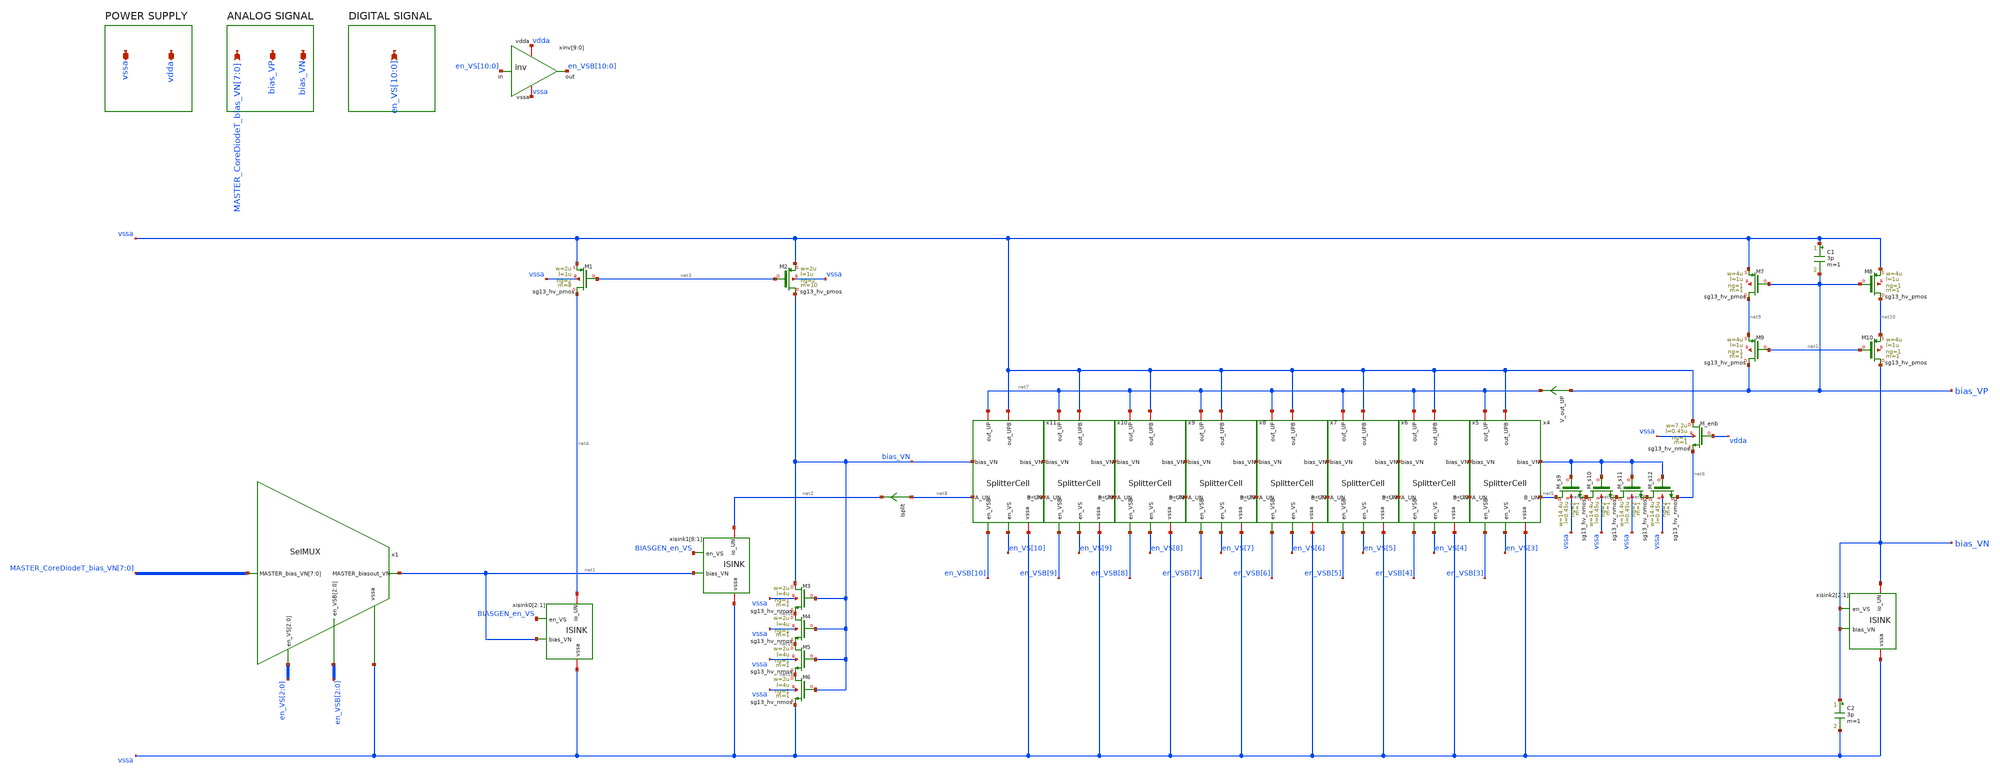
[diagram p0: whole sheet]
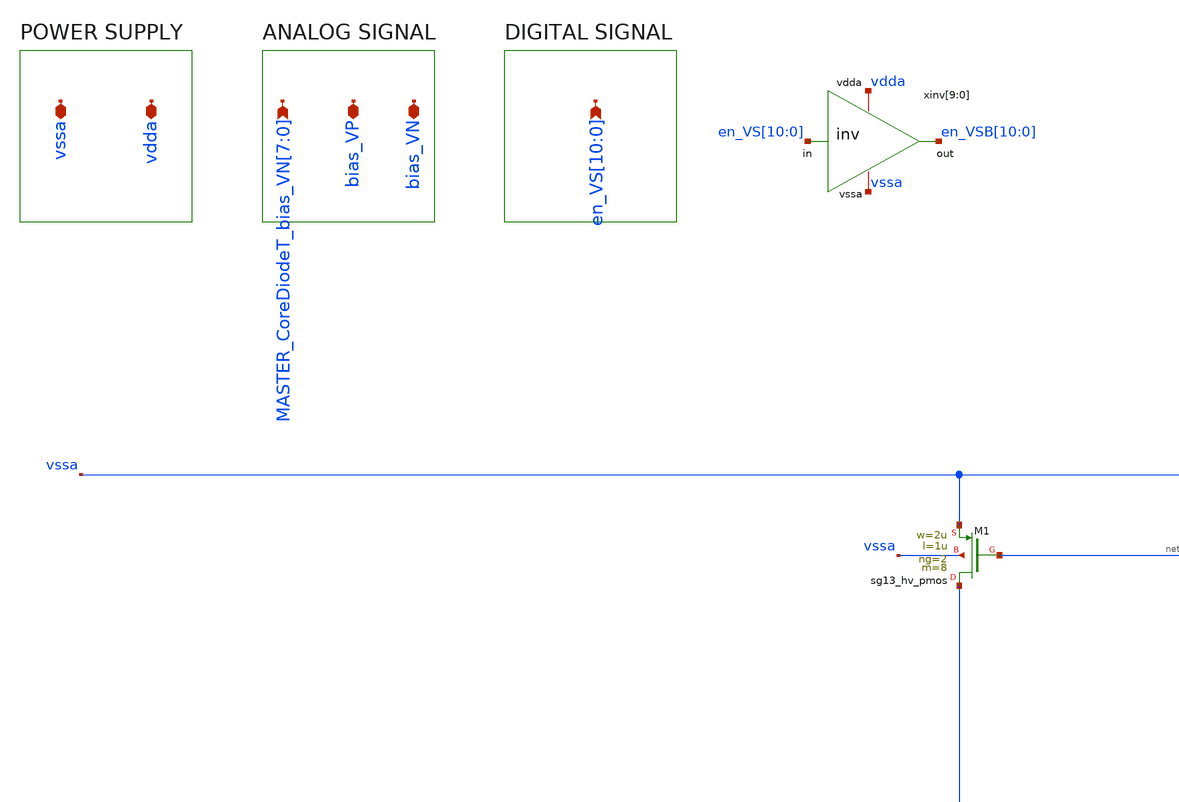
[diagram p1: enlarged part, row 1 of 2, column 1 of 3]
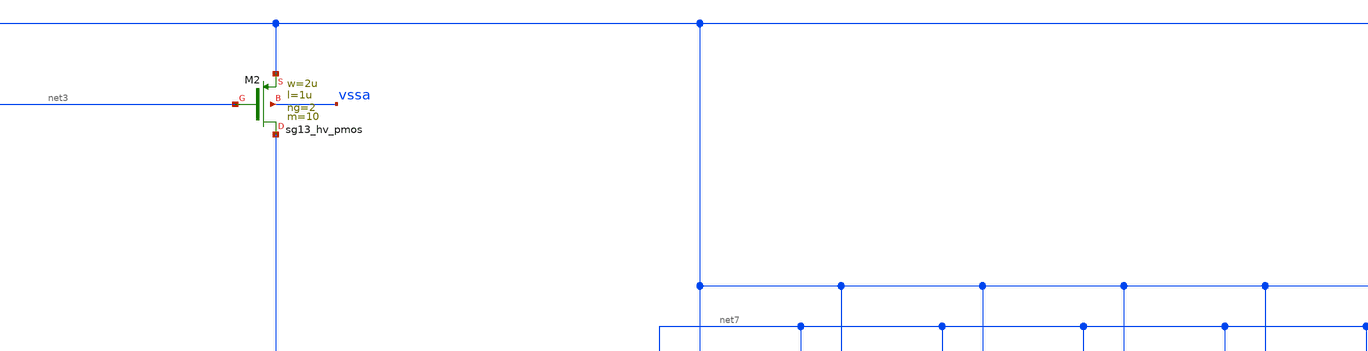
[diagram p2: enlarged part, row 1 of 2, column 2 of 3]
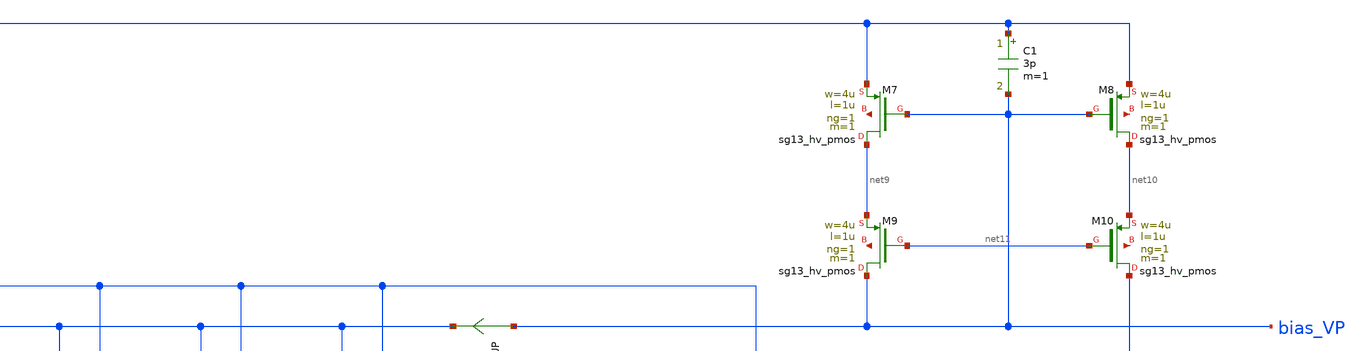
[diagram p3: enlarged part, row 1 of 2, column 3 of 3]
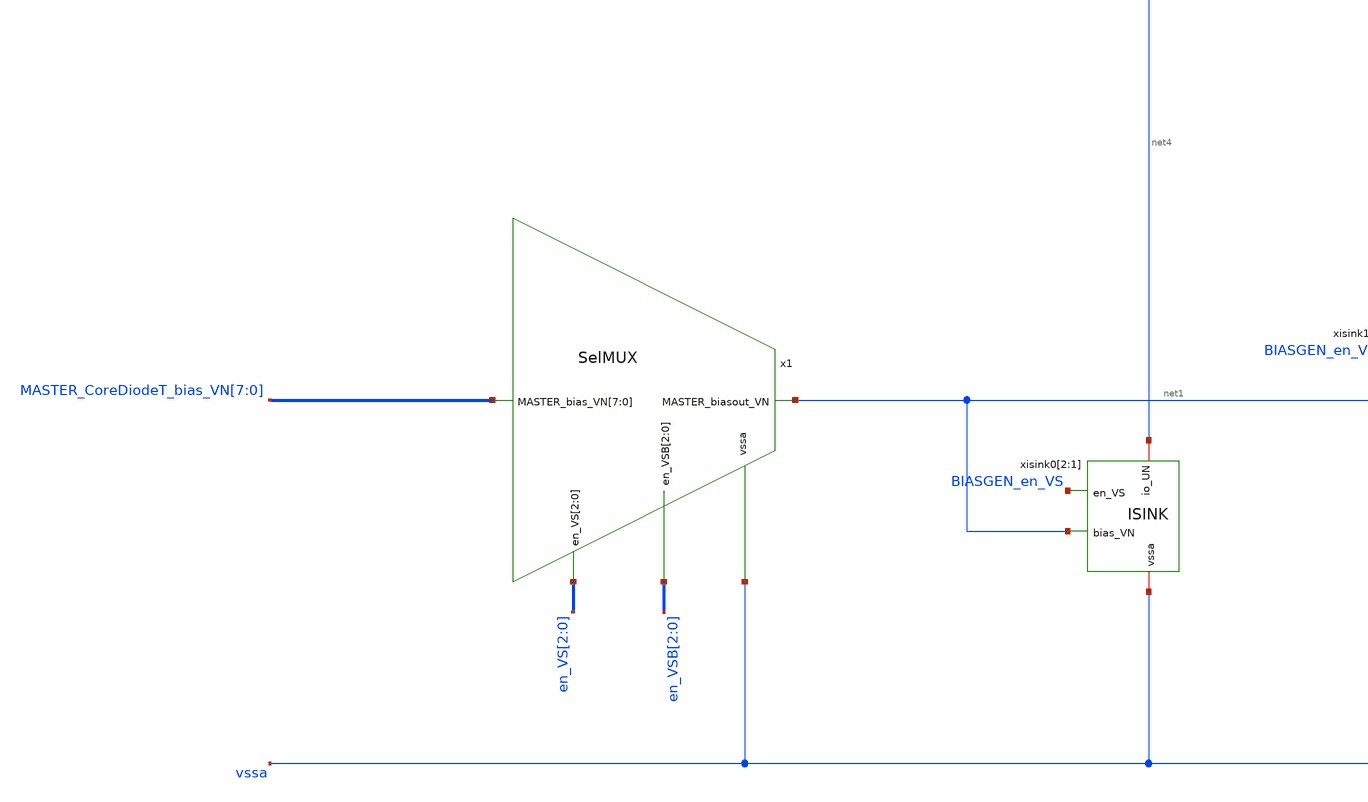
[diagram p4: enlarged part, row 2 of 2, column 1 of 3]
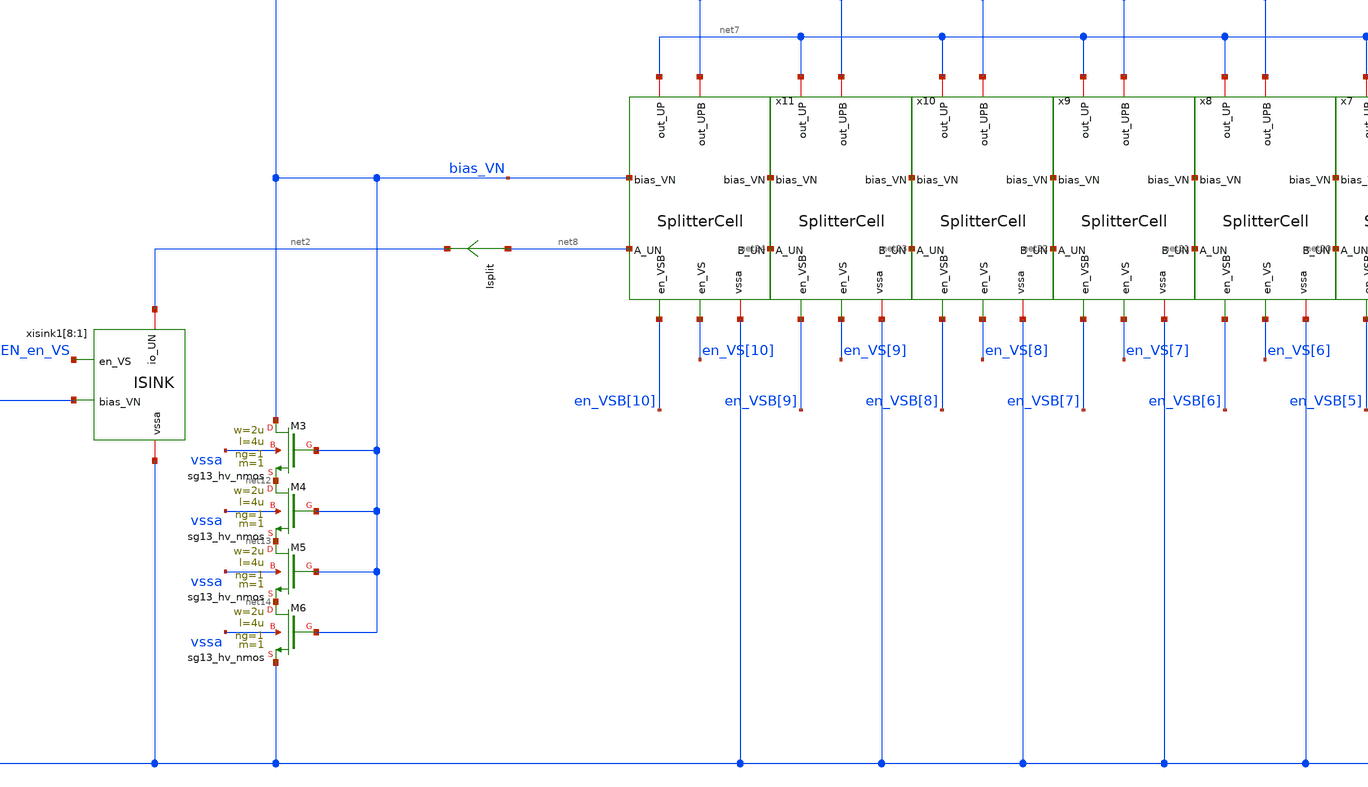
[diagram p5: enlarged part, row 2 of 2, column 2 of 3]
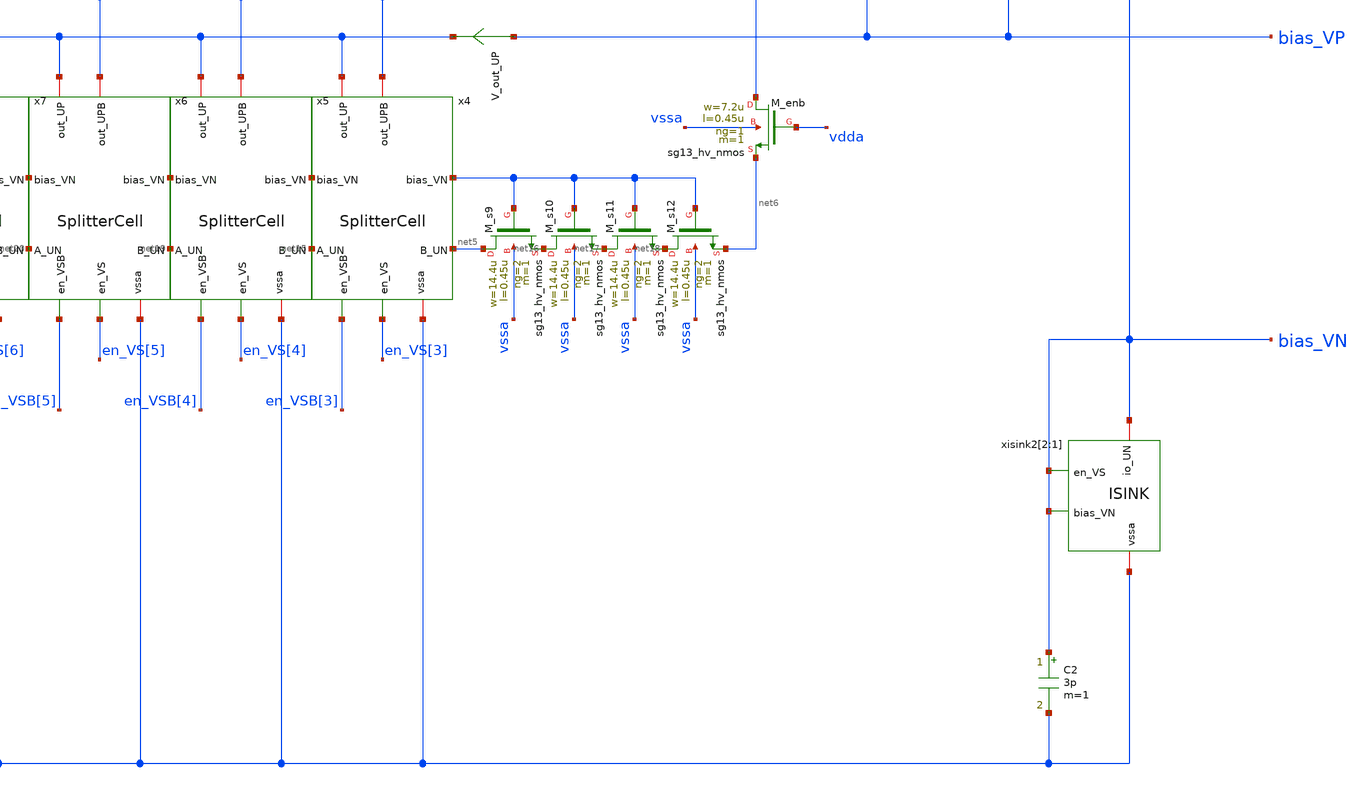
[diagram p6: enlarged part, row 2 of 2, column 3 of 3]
** sch_path: CoreFineDAC_N.sch
**.subckt CoreFineDAC_N
*+ MASTER_CoreDiodeT_bias_VN[7],MASTER_CoreDiodeT_bias_VN[6],MASTER_CoreDiodeT_bias_VN[5],MASTER_CoreDiodeT_bias_VN[4],MASTER_CoreDiodeT_bias_VN[3],MASTER_CoreDiodeT_bias_VN[2],MASTER_CoreDiodeT_bias_VN[1],MASTER_CoreDiodeT_bias_VN[0] en_VS[10],en_VS[9],en_VS[8],en_VS[7],en_VS[6],en_VS[5],en_VS[4],en_VS[3],en_VS[2],en_VS[1],en_VS[0]
*+ vssa vdda bias_VP bias_VN
*.ipin
*+ MASTER_CoreDiodeT_bias_VN[7],MASTER_CoreDiodeT_bias_VN[6],MASTER_CoreDiodeT_bias_VN[5],MASTER_CoreDiodeT_bias_VN[4],MASTER_CoreDiodeT_bias_VN[3],MASTER_CoreDiodeT_bias_VN[2],MASTER_CoreDiodeT_bias_VN[1],MASTER_CoreDiodeT_bias_VN[0]
*.ipin
*+ en_VS[10],en_VS[9],en_VS[8],en_VS[7],en_VS[6],en_VS[5],en_VS[4],en_VS[3],en_VS[2],en_VS[1],en_VS[0]
*.iopin vssa
*.iopin vdda
*.iopin bias_VP
*.iopin bias_VN
xinv[9] vdda en_VSB[10] en_VS[10] vssa inv
xinv[8] vdda en_VSB[9] en_VS[9] vssa inv
xinv[7] vdda en_VSB[8] en_VS[8] vssa inv
xinv[6] vdda en_VSB[7] en_VS[7] vssa inv
xinv[5] vdda en_VSB[6] en_VS[6] vssa inv
xinv[4] vdda en_VSB[5] en_VS[5] vssa inv
xinv[3] vdda en_VSB[4] en_VS[4] vssa inv
xinv[2] vdda en_VSB[3] en_VS[3] vssa inv
xinv[1] vdda en_VSB[2] en_VS[2] vssa inv
xinv[0] vdda en_VSB[1] en_VS[1] vssa inv
x1 MASTER_CoreDiodeT_bias_VN[7] MASTER_CoreDiodeT_bias_VN[6] MASTER_CoreDiodeT_bias_VN[5]
+ MASTER_CoreDiodeT_bias_VN[4] MASTER_CoreDiodeT_bias_VN[3] MASTER_CoreDiodeT_bias_VN[2] MASTER_CoreDiodeT_bias_VN[1]
+ MASTER_CoreDiodeT_bias_VN[0] vssa en_VS[2] en_VS[1] en_VS[0] en_VSB[2] en_VSB[1] en_VSB[0] net1 SelMUX
xisink0[2] net1 vssa BIASGEN_en_VS net4 ISINK
xisink0[1] net1 vssa BIASGEN_en_VS net4 ISINK
xisink1[8] net1 vssa BIASGEN_en_VS net2 ISINK
xisink1[7] net1 vssa BIASGEN_en_VS net2 ISINK
xisink1[6] net1 vssa BIASGEN_en_VS net2 ISINK
xisink1[5] net1 vssa BIASGEN_en_VS net2 ISINK
xisink1[4] net1 vssa BIASGEN_en_VS net2 ISINK
xisink1[3] net1 vssa BIASGEN_en_VS net2 ISINK
xisink1[2] net1 vssa BIASGEN_en_VS net2 ISINK
xisink1[1] net1 vssa BIASGEN_en_VS net2 ISINK
XM1 net4 net3 vssa vssa sg13_hv_pmos w=2u l=1u ng=2 m=8 mm_ok=1
XM2 bias_VN net3 vssa vssa sg13_hv_pmos w=2u l=1u ng=2 m=10 mm_ok=1
XM3 bias_VN bias_VN net12 vssa sg13_hv_nmos w=2u l=4u ng=1 m=1 mm_ok=1
XM4 net12 bias_VN net13 vssa sg13_hv_nmos w=2u l=4u ng=1 m=1 mm_ok=1
XM5 net13 bias_VN net14 vssa sg13_hv_nmos w=2u l=4u ng=1 m=1 mm_ok=1
XM6 net14 bias_VN vssa vssa sg13_hv_nmos w=2u l=4u ng=1 m=1 mm_ok=1
x4 en_VS[3] net15 net5 en_VSB[3] bias_VN vssa vssa net7 SplitterCell
XM_enb vssa vdda net6 vssa sg13_hv_nmos w=7.2u l=0.45u ng=1 m=1 mm_ok=1
XM_s9 net5 bias_VN net16 vssa sg13_hv_nmos w=14.4u l=0.45u ng=2 m=1 mm_ok=1
XM_s10 net16 bias_VN net17 vssa sg13_hv_nmos w=14.4u l=0.45u ng=2 m=1 mm_ok=1
XM_s11 net17 bias_VN net18 vssa sg13_hv_nmos w=14.4u l=0.45u ng=2 m=1 mm_ok=1
XM_s12 net18 bias_VN net6 vssa sg13_hv_nmos w=14.4u l=0.45u ng=2 m=1 mm_ok=1
V_out_UP bias_VP net7 0
.save i(v_out_up)
x5 en_VS[4] net19 net15 en_VSB[4] bias_VN vssa vssa net7 SplitterCell
x6 en_VS[5] net20 net19 en_VSB[5] bias_VN vssa vssa net7 SplitterCell
x7 en_VS[6] net21 net20 en_VSB[6] bias_VN vssa vssa net7 SplitterCell
x8 en_VS[7] net22 net21 en_VSB[7] bias_VN vssa vssa net7 SplitterCell
x9 en_VS[8] net23 net22 en_VSB[8] bias_VN vssa vssa net7 SplitterCell
x10 en_VS[9] net24 net23 en_VSB[9] bias_VN vssa vssa net7 SplitterCell
x11 en_VS[10] net8 net24 en_VSB[10] bias_VN vssa vssa net7 SplitterCell
Isplit net8 net2 0
.save i(isplit)
XM7 net9 bias_VP vssa net25 sg13_hv_pmos w=4u l=1u ng=1 m=1 mm_ok=1
XM8 net10 bias_VP vssa net26 sg13_hv_pmos w=4u l=1u ng=1 m=1 mm_ok=1
XM9 bias_VP net11 net9 net27 sg13_hv_pmos w=4u l=1u ng=1 m=1 mm_ok=1
XM10 bias_VN net11 net10 net28 sg13_hv_pmos w=4u l=1u ng=1 m=1 mm_ok=1
C1 vssa bias_VP 3p m=1
xisink2[2] bias_VN vssa bias_VN bias_VN ISINK
xisink2[1] bias_VN vssa bias_VN bias_VN ISINK
C2 bias_VN vssa 3p m=1
**.ends
.end
